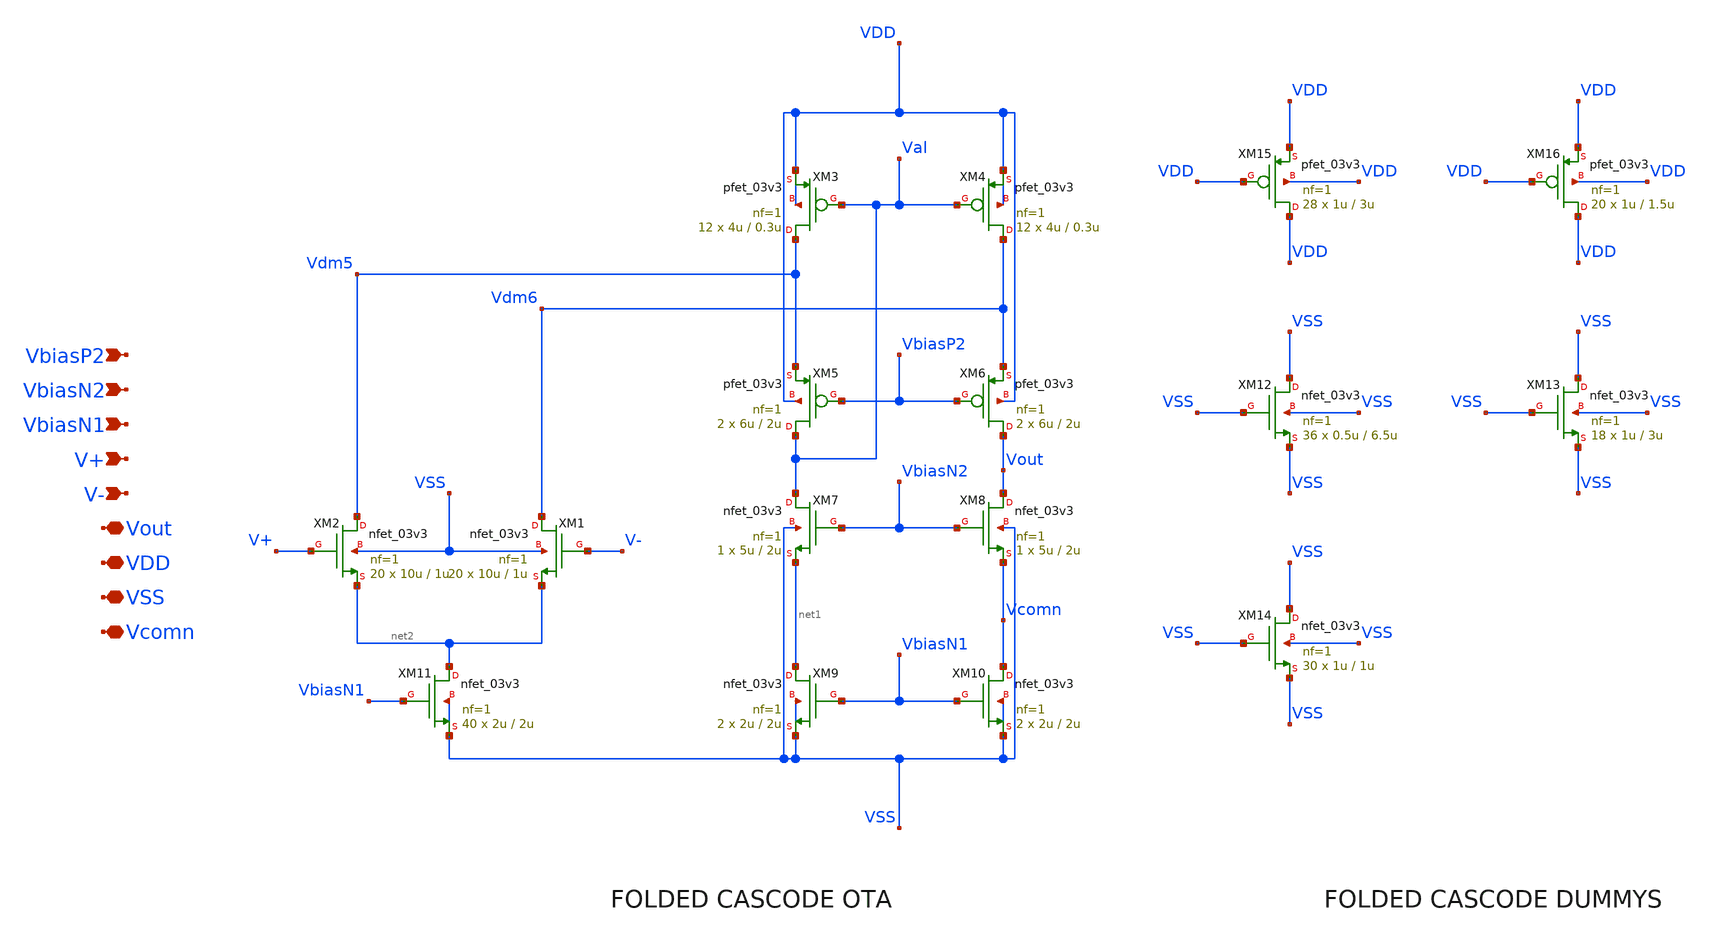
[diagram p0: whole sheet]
** sch_path: blocks/composite/folded_cascode/designs/gf180/error_amplifier_core_N_input/xschem/error_amplifier_core_N_input.sch
**.subckt error_amplifier_core_N_input VbiasN2 VDD VbiasP2 VbiasN1 V+ V- VSS Vcomn Vout
*.ipin VbiasN2
*.iopin VDD
*.ipin VbiasP2
*.ipin VbiasN1
*.ipin V+
*.ipin V-
*.iopin VSS
*.iopin Vcomn
*.iopin Vout
XM4 Vdm6 Val VDD VDD pfet_03v3 L=0.3u W=4u nf=1 ad='int((nf+1)/2) * W/nf * 0.18u' as='int((nf+2)/2) * W/nf * 0.18u'
+ pd='2*int((nf+1)/2) * (W/nf + 0.18u)' ps='2*int((nf+2)/2) * (W/nf + 0.18u)' nrd='0.18u / W' nrs='0.18u / W'
+ sa=0 sb=0 sd=0 m=12
XM3 Vdm5 Val VDD VDD pfet_03v3 L=0.3u W=4u nf=1 ad='int((nf+1)/2) * W/nf * 0.18u' as='int((nf+2)/2) * W/nf * 0.18u'
+ pd='2*int((nf+1)/2) * (W/nf + 0.18u)' ps='2*int((nf+2)/2) * (W/nf + 0.18u)' nrd='0.18u / W' nrs='0.18u / W'
+ sa=0 sb=0 sd=0 m=12
XM5 Val VbiasP2 Vdm5 VDD pfet_03v3 L=2u W=6u nf=1 ad='int((nf+1)/2) * W/nf * 0.18u' as='int((nf+2)/2) * W/nf * 0.18u'
+ pd='2*int((nf+1)/2) * (W/nf + 0.18u)' ps='2*int((nf+2)/2) * (W/nf + 0.18u)' nrd='0.18u / W' nrs='0.18u / W'
+ sa=0 sb=0 sd=0 m=2
XM6 Vout VbiasP2 Vdm6 VDD pfet_03v3 L=2u W=6u nf=1 ad='int((nf+1)/2) * W/nf * 0.18u' as='int((nf+2)/2) * W/nf * 0.18u'
+ pd='2*int((nf+1)/2) * (W/nf + 0.18u)' ps='2*int((nf+2)/2) * (W/nf + 0.18u)' nrd='0.18u / W' nrs='0.18u / W'
+ sa=0 sb=0 sd=0 m=2
XM9 net1 VbiasN1 VSS VSS nfet_03v3 L=2u W=2u nf=1 ad='int((nf+1)/2) * W/nf * 0.18u' as='int((nf+2)/2) * W/nf * 0.18u'
+ pd='2*int((nf+1)/2) * (W/nf + 0.18u)' ps='2*int((nf+2)/2) * (W/nf + 0.18u)' nrd='0.18u / W' nrs='0.18u / W'
+ sa=0 sb=0 sd=0 m=2
XM8 Vout VbiasN2 Vcomn VSS nfet_03v3 L=2u W=5u nf=1 ad='int((nf+1)/2) * W/nf * 0.18u' as='int((nf+2)/2) * W/nf * 0.18u'
+ pd='2*int((nf+1)/2) * (W/nf + 0.18u)' ps='2*int((nf+2)/2) * (W/nf + 0.18u)' nrd='0.18u / W' nrs='0.18u / W'
+ sa=0 sb=0 sd=0 m=1
XM7 Val VbiasN2 net1 VSS nfet_03v3 L=2u W=5u nf=1 ad='int((nf+1)/2) * W/nf * 0.18u' as='int((nf+2)/2) * W/nf * 0.18u'
+ pd='2*int((nf+1)/2) * (W/nf + 0.18u)' ps='2*int((nf+2)/2) * (W/nf + 0.18u)' nrd='0.18u / W' nrs='0.18u / W'
+ sa=0 sb=0 sd=0 m=1
XM10 Vcomn VbiasN1 VSS VSS nfet_03v3 L=2u W=2u nf=1 ad='int((nf+1)/2) * W/nf * 0.18u' as='int((nf+2)/2) * W/nf * 0.18u'
+ pd='2*int((nf+1)/2) * (W/nf + 0.18u)' ps='2*int((nf+2)/2) * (W/nf + 0.18u)' nrd='0.18u / W' nrs='0.18u / W'
+ sa=0 sb=0 sd=0 m=2
XM15 VDD VDD VDD VDD pfet_03v3 L=3u W=1u nf=1 ad='int((nf+1)/2) * W/nf * 0.18u' as='int((nf+2)/2) * W/nf * 0.18u'
+ pd='2*int((nf+1)/2) * (W/nf + 0.18u)' ps='2*int((nf+2)/2) * (W/nf + 0.18u)' nrd='0.18u / W' nrs='0.18u / W'
+ sa=0 sb=0 sd=0 m=28
XM16 VDD VDD VDD VDD pfet_03v3 L=1.5u W=1u nf=1 ad='int((nf+1)/2) * W/nf * 0.18u' as='int((nf+2)/2) * W/nf * 0.18u'
+ pd='2*int((nf+1)/2) * (W/nf + 0.18u)' ps='2*int((nf+2)/2) * (W/nf + 0.18u)' nrd='0.18u / W' nrs='0.18u / W'
+ sa=0 sb=0 sd=0 m=20
XM13 VSS VSS VSS VSS nfet_03v3 L=3u W=1u nf=1 ad='int((nf+1)/2) * W/nf * 0.18u' as='int((nf+2)/2) * W/nf * 0.18u'
+ pd='2*int((nf+1)/2) * (W/nf + 0.18u)' ps='2*int((nf+2)/2) * (W/nf + 0.18u)' nrd='0.18u / W' nrs='0.18u / W'
+ sa=0 sb=0 sd=0 m=18
XM12 VSS VSS VSS VSS nfet_03v3 L=6.5u W=0.5u nf=1 ad='int((nf+1)/2) * W/nf * 0.18u' as='int((nf+2)/2) * W/nf * 0.18u'
+ pd='2*int((nf+1)/2) * (W/nf + 0.18u)' ps='2*int((nf+2)/2) * (W/nf + 0.18u)' nrd='0.18u / W' nrs='0.18u / W'
+ sa=0 sb=0 sd=0 m=36
XM14 VSS VSS VSS VSS nfet_03v3 L=1u W=1u nf=1 ad='int((nf+1)/2) * W/nf * 0.18u' as='int((nf+2)/2) * W/nf * 0.18u'
+ pd='2*int((nf+1)/2) * (W/nf + 0.18u)' ps='2*int((nf+2)/2) * (W/nf + 0.18u)' nrd='0.18u / W' nrs='0.18u / W'
+ sa=0 sb=0 sd=0 m=30
XM1 Vdm6 V- net2 VSS nfet_03v3 L=1u W=10u nf=1 ad='int((nf+1)/2) * W/nf * 0.18u' as='int((nf+2)/2) * W/nf * 0.18u'
+ pd='2*int((nf+1)/2) * (W/nf + 0.18u)' ps='2*int((nf+2)/2) * (W/nf + 0.18u)' nrd='0.18u / W' nrs='0.18u / W'
+ sa=0 sb=0 sd=0 m=20
XM2 Vdm5 V+ net2 VSS nfet_03v3 L=1u W=10u nf=1 ad='int((nf+1)/2) * W/nf * 0.18u' as='int((nf+2)/2) * W/nf * 0.18u'
+ pd='2*int((nf+1)/2) * (W/nf + 0.18u)' ps='2*int((nf+2)/2) * (W/nf + 0.18u)' nrd='0.18u / W' nrs='0.18u / W'
+ sa=0 sb=0 sd=0 m=20
XM11 net2 VbiasN1 VSS VSS nfet_03v3 L=2u W=2u nf=1 ad='int((nf+1)/2) * W/nf * 0.18u' as='int((nf+2)/2) * W/nf * 0.18u'
+ pd='2*int((nf+1)/2) * (W/nf + 0.18u)' ps='2*int((nf+2)/2) * (W/nf + 0.18u)' nrd='0.18u / W' nrs='0.18u / W'
+ sa=0 sb=0 sd=0 m=40
**.ends
.end
